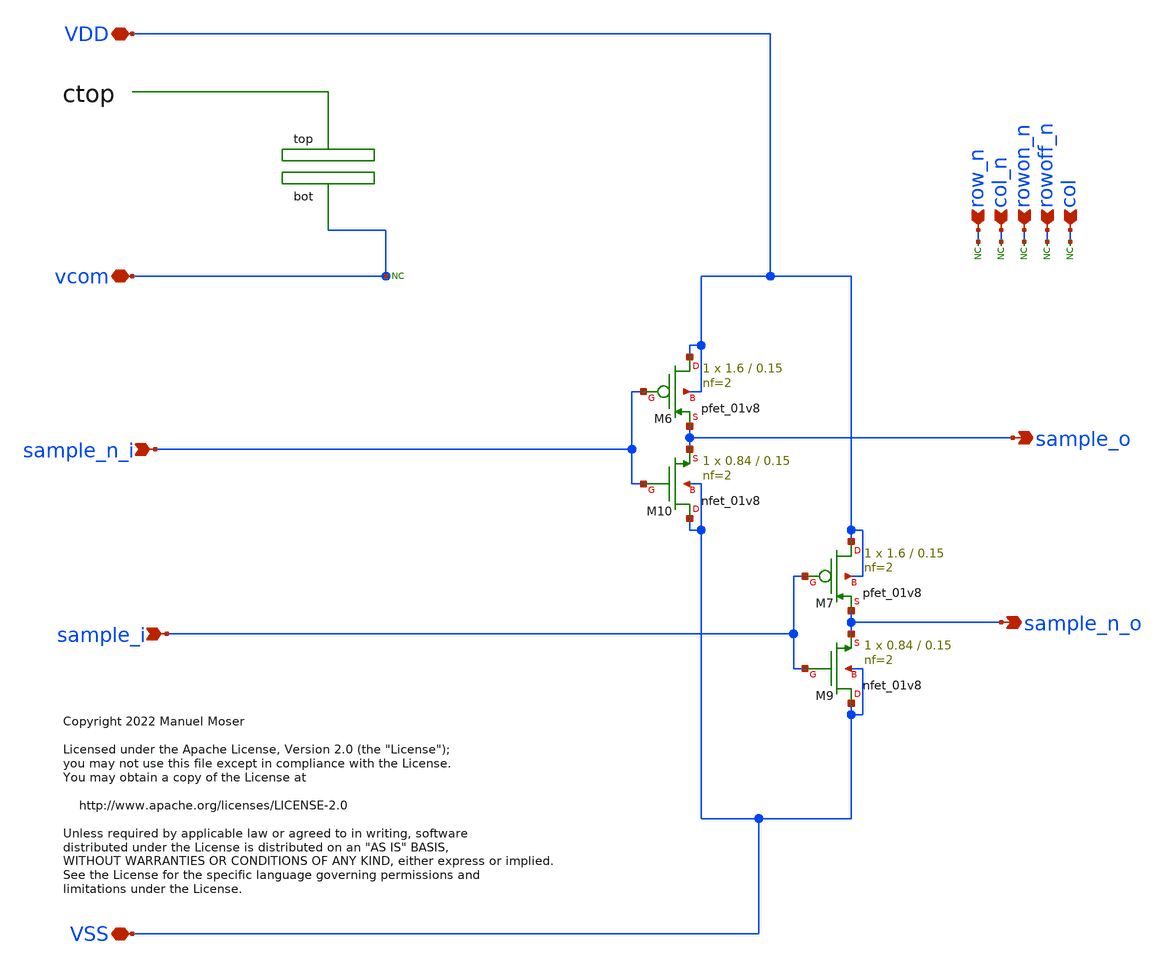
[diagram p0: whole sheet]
** sch_path: xschem/adc_array_circuit_drv.sch
* Copyright 2022 Manuel Moser
* Licensed under the Apache License, Version 2.0 (the "License");
**.subckt adc_array_circuit_drv sample_n_i sample_i vcom row_n col_n rowon_n VDD VSS sample_o
*+ sample_n_o rowoff_n col
*.ipin sample_n_i
*.ipin sample_i
*.iopin vcom
*.ipin row_n
*.ipin col_n
*.ipin rowon_n
*.iopin VDD
*.iopin VSS
*.opin sample_o
*.opin sample_n_o
*.ipin rowoff_n
*.ipin col
XM6 VDD sample_n_i sample_o VDD sky130_fd_pr__pfet_01v8 L=0.15 W=1.6 nf=2 ad='int((nf+1)/2) * W/nf * 0.29'
+ as='int((nf+2)/2) * W/nf * 0.29' pd='2*int((nf+1)/2) * (W/nf + 0.29)' ps='2*int((nf+2)/2) * (W/nf + 0.29)'
+ nrd='0.29 / W' nrs='0.29 / W' sa=0 sb=0 sd=0 mult=1 m=1
XM7 VDD sample_i sample_n_o VDD sky130_fd_pr__pfet_01v8 L=0.15 W=1.6 nf=2 ad='int((nf+1)/2) * W/nf * 0.29'
+ as='int((nf+2)/2) * W/nf * 0.29' pd='2*int((nf+1)/2) * (W/nf + 0.29)' ps='2*int((nf+2)/2) * (W/nf + 0.29)'
+ nrd='0.29 / W' nrs='0.29 / W' sa=0 sb=0 sd=0 mult=1 m=1
XM9 VSS sample_i sample_n_o VSS sky130_fd_pr__nfet_01v8 L=0.15 W=0.84 nf=2 ad='int((nf+1)/2) * W/nf * 0.29'
+ as='int((nf+2)/2) * W/nf * 0.29' pd='2*int((nf+1)/2) * (W/nf + 0.29)' ps='2*int((nf+2)/2) * (W/nf + 0.29)'
+ nrd='0.29 / W' nrs='0.29 / W' sa=0 sb=0 sd=0 mult=1 m=1
XM10 VSS sample_n_i sample_o VSS sky130_fd_pr__nfet_01v8 L=0.15 W=0.84 nf=2 ad='int((nf+1)/2) * W/nf * 0.29'
+ as='int((nf+2)/2) * W/nf * 0.29' pd='2*int((nf+1)/2) * (W/nf + 0.29)' ps='2*int((nf+2)/2) * (W/nf + 0.29)'
+ nrd='0.29 / W' nrs='0.29 / W' sa=0 sb=0 sd=0 mult=1 m=1
* noconn row_n
* noconn col_n
* noconn rowon_n
* noconn vcom
* noconn rowoff_n
* noconn col
**.ends
.end
